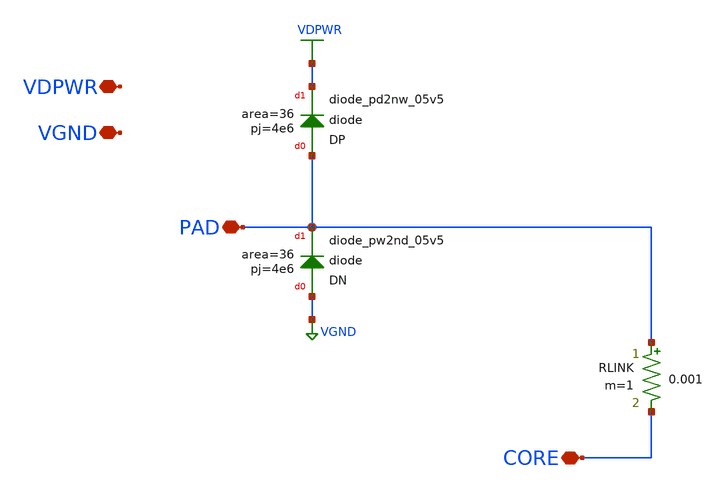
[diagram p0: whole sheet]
** sch_path: cells/ELAD1_PINPROT/schematic/ELAD1_PINPROT.sch
**.subckt ELAD1_PINPROT PAD CORE VDPWR VGND
*.iopin PAD
*.iopin CORE
*.iopin VDPWR
*.iopin VGND
RLINK PAD CORE 0.001 m=1
XDN VGND PAD sky130_fd_pr__diode_pw2nd_05v5 area=36 pj=4e6
XDP PAD VDPWR sky130_fd_pr__diode_pd2nw_05v5 area=36 pj=4e6
**.ends
.GLOBAL VGND
.GLOBAL VDPWR
.end
